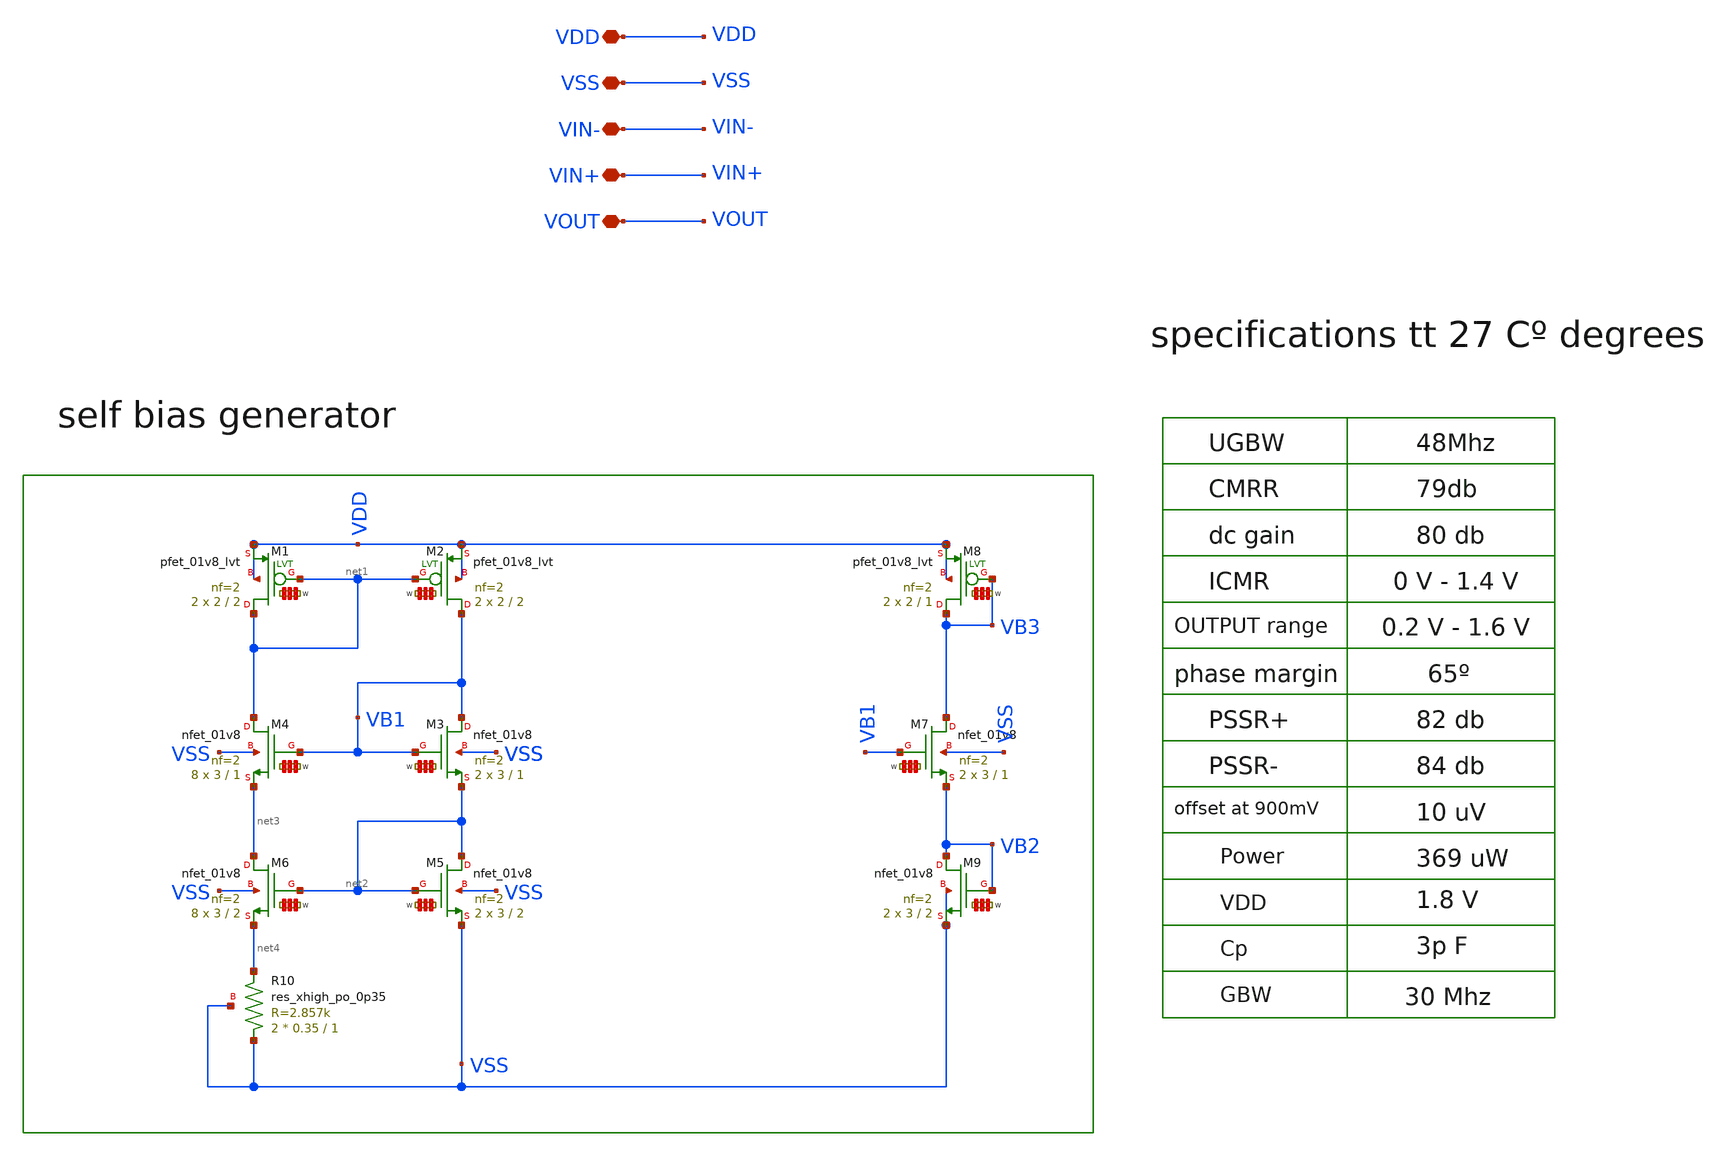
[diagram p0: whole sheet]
** sch_path: my_ip/LIB/VA002_NMOS_1.8_sky130A.sch
**.subckt VA002_NMOS_1.8_sky130A VDD VSS VIN- VIN+ VOUT
*.iopin VDD
*.iopin VSS
*.iopin VIN-
*.iopin VIN+
*.iopin VOUT
XR10 VSS net4 VSS sky130_fd_pr__res_xhigh_po_0p35 L=1 mult=2 m=2
XM4 net1 VB1 net3 VSS sky130_fd_pr__nfet_01v8 L=1 W='3 * 2 ' nf=2 ad='int((2 + 1)/2) * 3 / 2 * 0.29'
+ as='int((2 + 2)/2) * 3 / 2 * 0.29' pd='2*int((2 + 1)/2) * (3 / 2 + 0.29)' ps='2*int((2 + 2)/2) * (3 / 2 + 0.29)'
+ nrd='0.29 / 3 ' nrs='0.29 / 3 ' sa=0 sb=0 sd=0 mult=8 m=8
XM3 VB1 VB1 net2 VSS sky130_fd_pr__nfet_01v8 L=1 W='3 * 2 ' nf=2 ad='int((2 + 1)/2) * 3 / 2 * 0.29' as='int((2 + 2)/2) * 3 / 2 * 0.29'
+ pd='2*int((2 + 1)/2) * (3 / 2 + 0.29)' ps='2*int((2 + 2)/2) * (3 / 2 + 0.29)' nrd='0.29 / 3 ' nrs='0.29 / 3 '
+ sa=0 sb=0 sd=0 mult=2 m=2
XM6 net3 net2 net4 VSS sky130_fd_pr__nfet_01v8 L=2 W='3 * 2 ' nf=2 ad='int((2 + 1)/2) * 3 / 2 * 0.29'
+ as='int((2 + 2)/2) * 3 / 2 * 0.29' pd='2*int((2 + 1)/2) * (3 / 2 + 0.29)' ps='2*int((2 + 2)/2) * (3 / 2 + 0.29)'
+ nrd='0.29 / 3 ' nrs='0.29 / 3 ' sa=0 sb=0 sd=0 mult=8 m=8
XM5 net2 net2 VSS VSS sky130_fd_pr__nfet_01v8 L=2 W='3 * 2 ' nf=2 ad='int((2 + 1)/2) * 3 / 2 * 0.29'
+ as='int((2 + 2)/2) * 3 / 2 * 0.29' pd='2*int((2 + 1)/2) * (3 / 2 + 0.29)' ps='2*int((2 + 2)/2) * (3 / 2 + 0.29)'
+ nrd='0.29 / 3 ' nrs='0.29 / 3 ' sa=0 sb=0 sd=0 mult=2 m=2
XM7 VB3 VB1 VB2 VSS sky130_fd_pr__nfet_01v8 L=1 W='3 * 2 ' nf=2 ad='int((2 + 1)/2) * 3 / 2 * 0.29' as='int((2 + 2)/2) * 3 / 2 * 0.29'
+ pd='2*int((2 + 1)/2) * (3 / 2 + 0.29)' ps='2*int((2 + 2)/2) * (3 / 2 + 0.29)' nrd='0.29 / 3 ' nrs='0.29 / 3 '
+ sa=0 sb=0 sd=0 mult=2 m=2
XM9 VB2 VB2 VSS VSS sky130_fd_pr__nfet_01v8 L=2 W='3 * 2 ' nf=2 ad='int((2 + 1)/2) * 3 / 2 * 0.29' as='int((2 + 2)/2) * 3 / 2 * 0.29'
+ pd='2*int((2 + 1)/2) * (3 / 2 + 0.29)' ps='2*int((2 + 2)/2) * (3 / 2 + 0.29)' nrd='0.29 / 3 ' nrs='0.29 / 3 '
+ sa=0 sb=0 sd=0 mult=2 m=2
XM8 VB3 VB3 VDD VDD sky130_fd_pr__pfet_01v8_lvt L=1 W='2 * 2 ' nf=2 ad='int((2 + 1)/2) * 2 / 2 * 0.29'
+ as='int((2 + 2)/2) * 2 / 2 * 0.29' pd='2*int((2 + 1)/2) * (2 / 2 + 0.29)' ps='2*int((2 + 2)/2) * (2 / 2 + 0.29)'
+ nrd='0.29 / 2 ' nrs='0.29 / 2 ' sa=0 sb=0 sd=0 mult=2 m=2
XM1 net1 net1 VDD VDD sky130_fd_pr__pfet_01v8_lvt L=2 W='2 * 2 ' nf=2 ad='int((2 + 1)/2) * 2 / 2 * 0.29'
+ as='int((2 + 2)/2) * 2 / 2 * 0.29' pd='2*int((2 + 1)/2) * (2 / 2 + 0.29)' ps='2*int((2 + 2)/2) * (2 / 2 + 0.29)'
+ nrd='0.29 / 2 ' nrs='0.29 / 2 ' sa=0 sb=0 sd=0 mult=2 m=2
XM2 VB1 net1 VDD VDD sky130_fd_pr__pfet_01v8_lvt L=2 W='2 * 2 ' nf=2 ad='int((2 + 1)/2) * 2 / 2 * 0.29'
+ as='int((2 + 2)/2) * 2 / 2 * 0.29' pd='2*int((2 + 1)/2) * (2 / 2 + 0.29)' ps='2*int((2 + 2)/2) * (2 / 2 + 0.29)'
+ nrd='0.29 / 2 ' nrs='0.29 / 2 ' sa=0 sb=0 sd=0 mult=2 m=2
**.ends
.end
